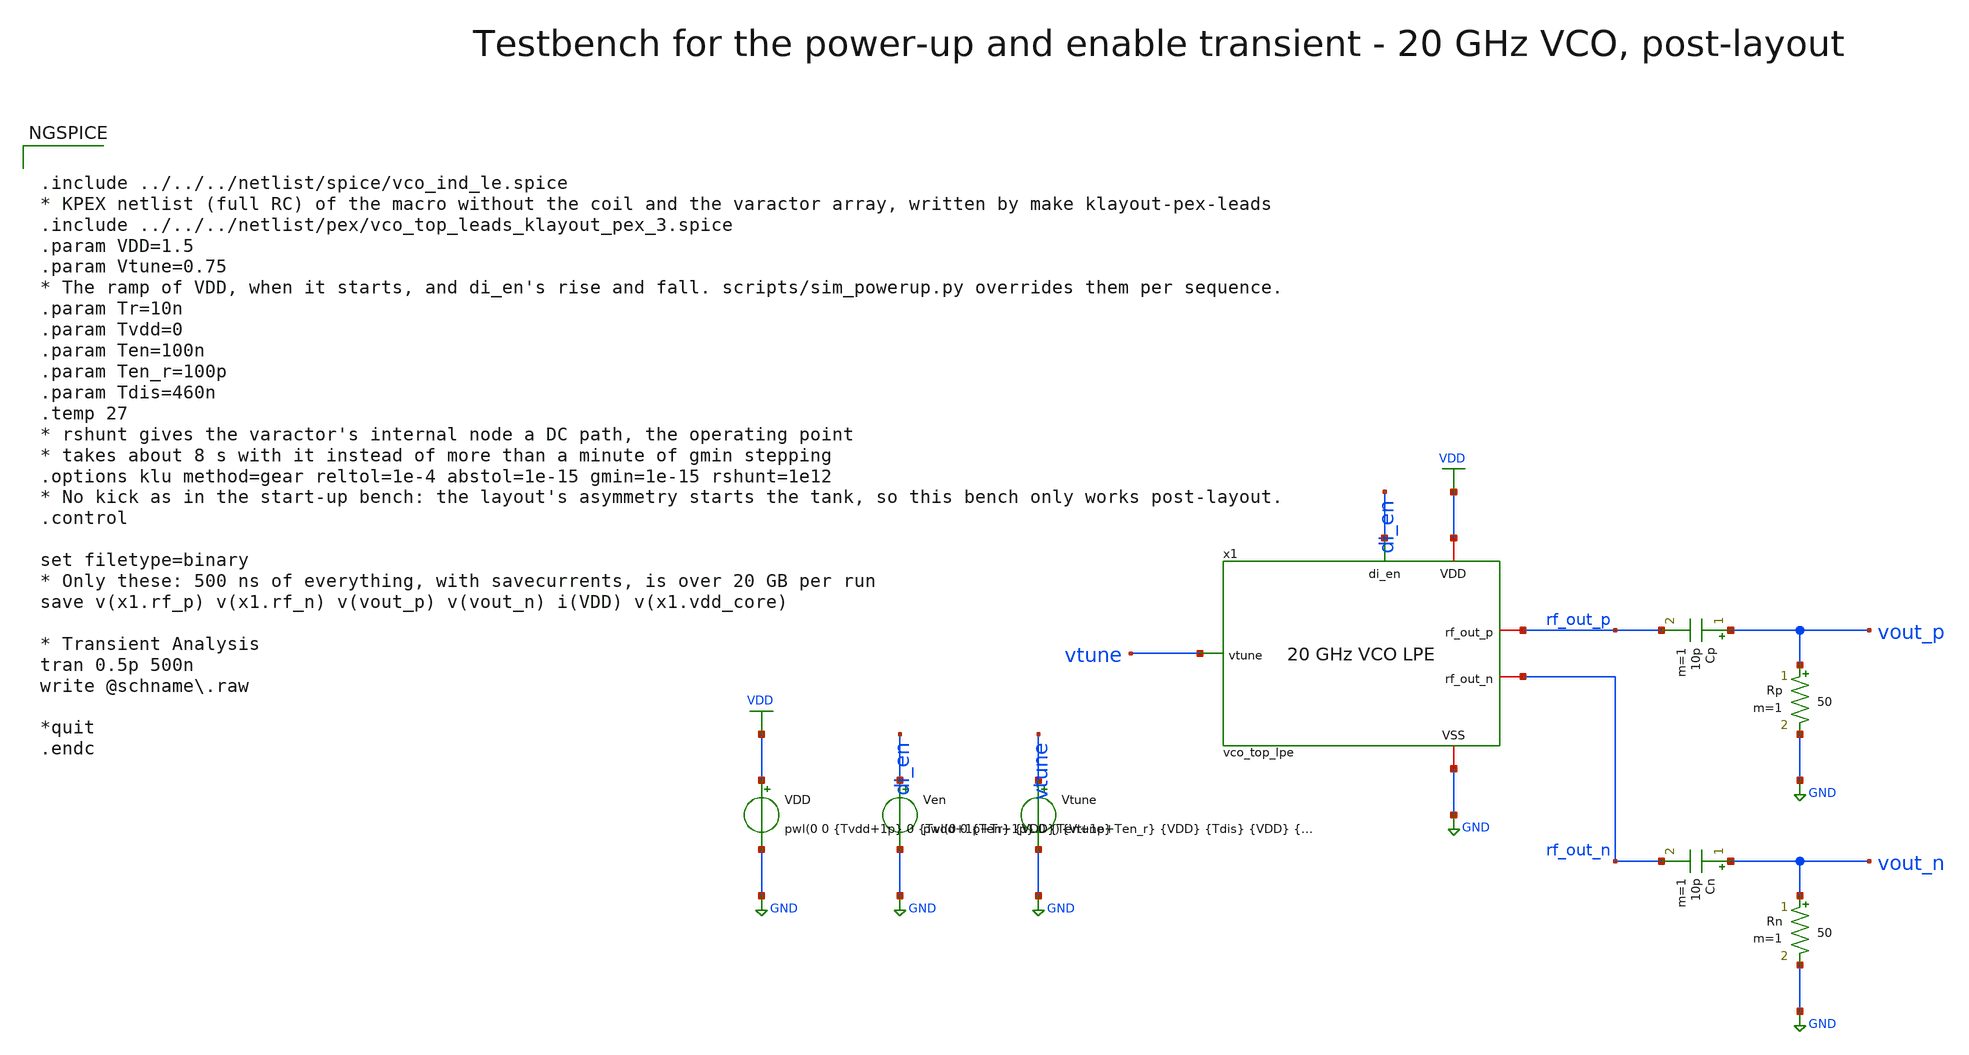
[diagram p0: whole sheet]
** sch_path: macros/vco/testbenches/xschem/vco_top_tb_powerup_lpe.sch
**.subckt vco_top_tb_powerup_lpe
x1 di_en VDD GND vtune rf_out_p rf_out_n vco_top_lpe
Cp vout_p rf_out_p 10p m=1
Rp vout_p GND 50 m=1
Cn vout_n rf_out_n 10p m=1
Rn vout_n GND 50 m=1
VDD VDD GND pwl(0 0 {Tvdd+1p} 0 {Tvdd+1p+Tr} {VDD})
Ven di_en GND pwl(0 0 {Ten+1p} 0 {Ten+1p+Ten_r} {VDD} {Tdis} {VDD} {Tdis+100p} 0)
Vtune vtune GND {Vtune}
**** begin user architecture code


.include ../../../netlist/spice/vco_ind_le.spice
* KPEX netlist (full RC) of the macro without the coil and the varactor array, written by make
*+ klayout-pex-leads
.include ../../../netlist/pex/vco_top_leads_klayout_pex_3.spice
.param VDD=1.5
.param Vtune=0.75
* The ramp of VDD, when it starts, and di_en's rise and fall. scripts/sim_powerup.py overrides them per sequence.
.param Tr=10n
.param Tvdd=0
.param Ten=100n
.param Ten_r=100p
.param Tdis=460n
.temp 27
* rshunt gives the varactor's internal node a DC path, the operating point
* takes about 8 s with it instead of more than a minute of gmin stepping
.options klu method=gear reltol=1e-4 abstol=1e-15 gmin=1e-15 rshunt=1e12
* No kick as in the start-up bench: the layout's asymmetry starts the tank, so this bench only works post-layout.
.control

set filetype=binary
* Only these: 500 ns of everything, with savecurrents, is over 20 GB per run
save v(x1.rf_p) v(x1.rf_n) v(vout_p) v(vout_n) i(VDD) v(x1.vdd_core)

* Transient Analysis
tran 0.5p 500n
write @schname\.raw

*quit
.endc



.lib cornerMOSlv.lib mos_tt
.lib cornerMOShv.lib mos_tt
.lib cornerRES.lib res_typ
.lib cornerCAP.lib cap_typ

**** end user architecture code
**.ends

* expanding   symbol:  vco_top_lpe.sym # of pins=6
** sym_path: macros/vco/testbenches/xschem/vco_top_lpe.sym
** sch_path: macros/vco/testbenches/xschem/vco_top_lpe.sch
.subckt vco_top_lpe di_en VDD VSS vtune rf_out_p rf_out_n
*.iopin VDD
*.iopin VSS
*.ipin di_en
*.ipin vtune
*.iopin rf_out_p
*.iopin rf_out_n
xleads di_en vtune VDD VSS rf_out_p rf_out_n rf_p rf_n vdd_core vco_var_rf_p vco_var_rf_n vco_var_VSS vco_top_leads
xind rf_p rf_n vdd_core vco_ind_le
xvar vco_var_rf_p vco_var_rf_n vtune vco_var_VSS vco_var
.ends


* expanding   symbol:  vco_var.sym # of pins=4
** sym_path: macros/vco/schematic/xschem/vco_var.sym
** sch_path: macros/vco/schematic/xschem/vco_var.sch
.subckt vco_var rf_p rf_n vtune VSS
*.ipin vtune
*.iopin rf_p
*.iopin rf_n
*.iopin VSS
XCvar1 rf_p vtune rf_n VSS sg13_hv_svaricap w=3.74u l=0.3u Nx=7 mm_ok=1
XCvar2 rf_p vtune rf_n VSS sg13_hv_svaricap w=3.74u l=0.3u Nx=7 mm_ok=1
XCvar3 rf_p vtune rf_n VSS sg13_hv_svaricap w=3.74u l=0.3u Nx=7 mm_ok=1
.ends

.GLOBAL VDD
.GLOBAL GND
.end
